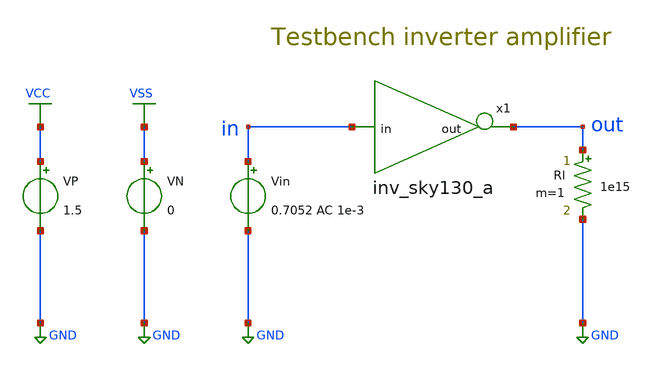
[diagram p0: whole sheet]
** sch_path: Amplifier_Inv/xschem/tb_inv_sky130_a.sch
* StefanSchippers/xschem_sky130/sky130_tests/not.sch:
* Copyright 2021 Stefan Frederik Schippers
* Licensed under the Apache License, Version 2.0 (the "License");
**.subckt tb_inv_sky130_a
x1 out in inv_sky130_a
VN VSS GND 0
VP VCC GND 1.5
Vin in GND 0.7052 AC 1e-3
Rl out GND 1e15 m=1
**** begin user architecture code

** opencircuitdesign pdks install
.lib $::SKYWATER_MODELS/sky130.lib.spice tt




.control
  save all
  ac dec 40 1 1e6
  let gain = db(v(out)/v(in))
  let phase = phase(v(out)/v(in))
  write tb_inv_sky130_a_AC.raw gain phase
  save all
.endc


**** end user architecture code
**.ends

* expanding   symbol:  inv_sky130_a.sym # of pins=2
** sym_path: Amplifier_Inv/xschem/inv_sky130_a.sym
** sch_path: Amplifier_Inv/xschem/inv_sky130_a.sch
.subckt inv_sky130_a out in
*.ipin in
*.opin out
x1 net1 in VCC VSS not W_N=20 L_N=0.15 W_P=40 L_P=0.15 m=1
XC1 out GND sky130_fd_pr__cap_mim_m3_1 W=15 L=15 MF=6 m=6
XR3 net1 in GND sky130_fd_pr__res_xhigh_po W=1 L=30 mult=1 m=1
XR1 out net1 GND sky130_fd_pr__res_xhigh_po W=1 L=50 mult=1 m=1
.ends


* expanding   symbol:  sky130_tests/not.sym # of pins=2
** sym_path: sky130_tests/not.sym
** sch_path: sky130_tests/not.sch
.subckt not y a VCCPIN VSSPIN     W_N=1 L_N=0.15 W_P=2 L_P=0.15
*.opin y
*.ipin a
XM1 DN a VSSPIN VSSPIN sky130_fd_pr__nfet_01v8 L=L_N W=W_N nf=1 ad='int((1 + 1)/2) * W_N / 1 * 0.29'
+ as='int((1 + 2)/2) * W_N / 1 * 0.29' pd='2*int((1 + 1)/2) * (W_N / 1 + 0.29)' ps='2*int((1 + 2)/2) * (W_N / 1 + 0.29)'
+ nrd='0.29 / W_N ' nrs='0.29 / W_N ' sa=0 sb=0 sd=0 mult=1 m=1
XM2 DP a VCCPIN VCCPIN sky130_fd_pr__pfet_01v8 L=L_P W=W_P nf=1 ad='int((nf+1)/2) * W/nf * 0.29' as='int((nf+2)/2) * W/nf * 0.29'
+ pd='2*int((nf+1)/2) * (W/nf + 0.29)' ps='2*int((nf+2)/2) * (W/nf + 0.29)' nrd='0.29 / W' nrs='0.29 / W'
+ sa=0 sb=0 sd=0 mult=1 m=1
Vmeas DP y 0
.save i(vmeas)
Vmeas1 y DN 0
.save i(vmeas1)
.save v(dp)
.save v(dn)
.ends

.GLOBAL GND
.GLOBAL VSS
.GLOBAL VCC
.end
